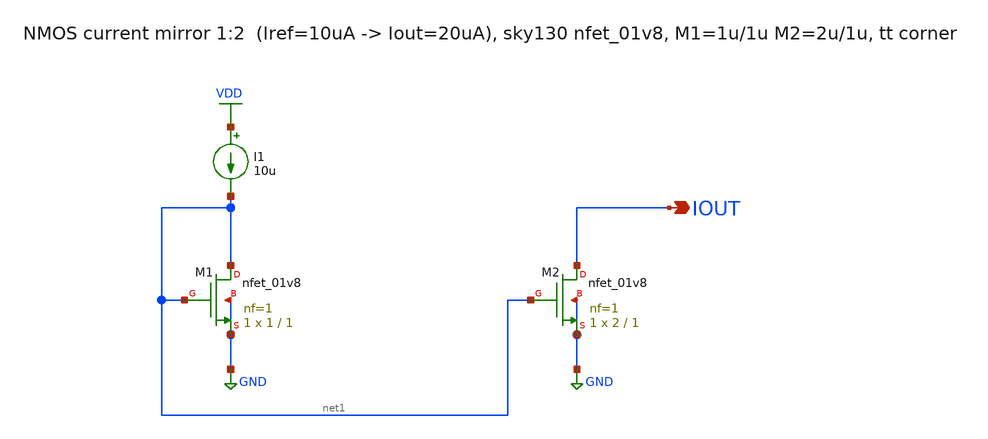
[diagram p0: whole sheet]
** sch_path: libraries/cal_runs/current_mirror/current_mirror.sch
**.subckt current_mirror IOUT
*.opin IOUT
XM1 net1 net1 GND GND sky130_fd_pr__nfet_01v8 L=1 W=1 nf=1 ad='int((1 + 1)/2) * 1 / 1 * 0.29' as='int((1 + 2)/2) * 1 / 1 * 0.29'
+ pd='2*int((1 + 1)/2) * (1 / 1 + 0.29)' ps='2*int((1 + 2)/2) * (1 / 1 + 0.29)' nrd='0.29 / 1 ' nrs='0.29 / 1 '
+ sa=0 sb=0 sd=0 mult=1 m=1
XM2 IOUT net1 GND GND sky130_fd_pr__nfet_01v8 L=1 W=2 nf=1 ad='int((1 + 1)/2) * 2 / 1 * 0.29' as='int((1 + 2)/2) * 2 / 1 * 0.29'
+ pd='2*int((1 + 1)/2) * (2 / 1 + 0.29)' ps='2*int((1 + 2)/2) * (2 / 1 + 0.29)' nrd='0.29 / 2 ' nrs='0.29 / 2 '
+ sa=0 sb=0 sd=0 mult=1 m=1
I1 VDD net1 10u
**.ends
.GLOBAL VDD
.GLOBAL GND
.end
